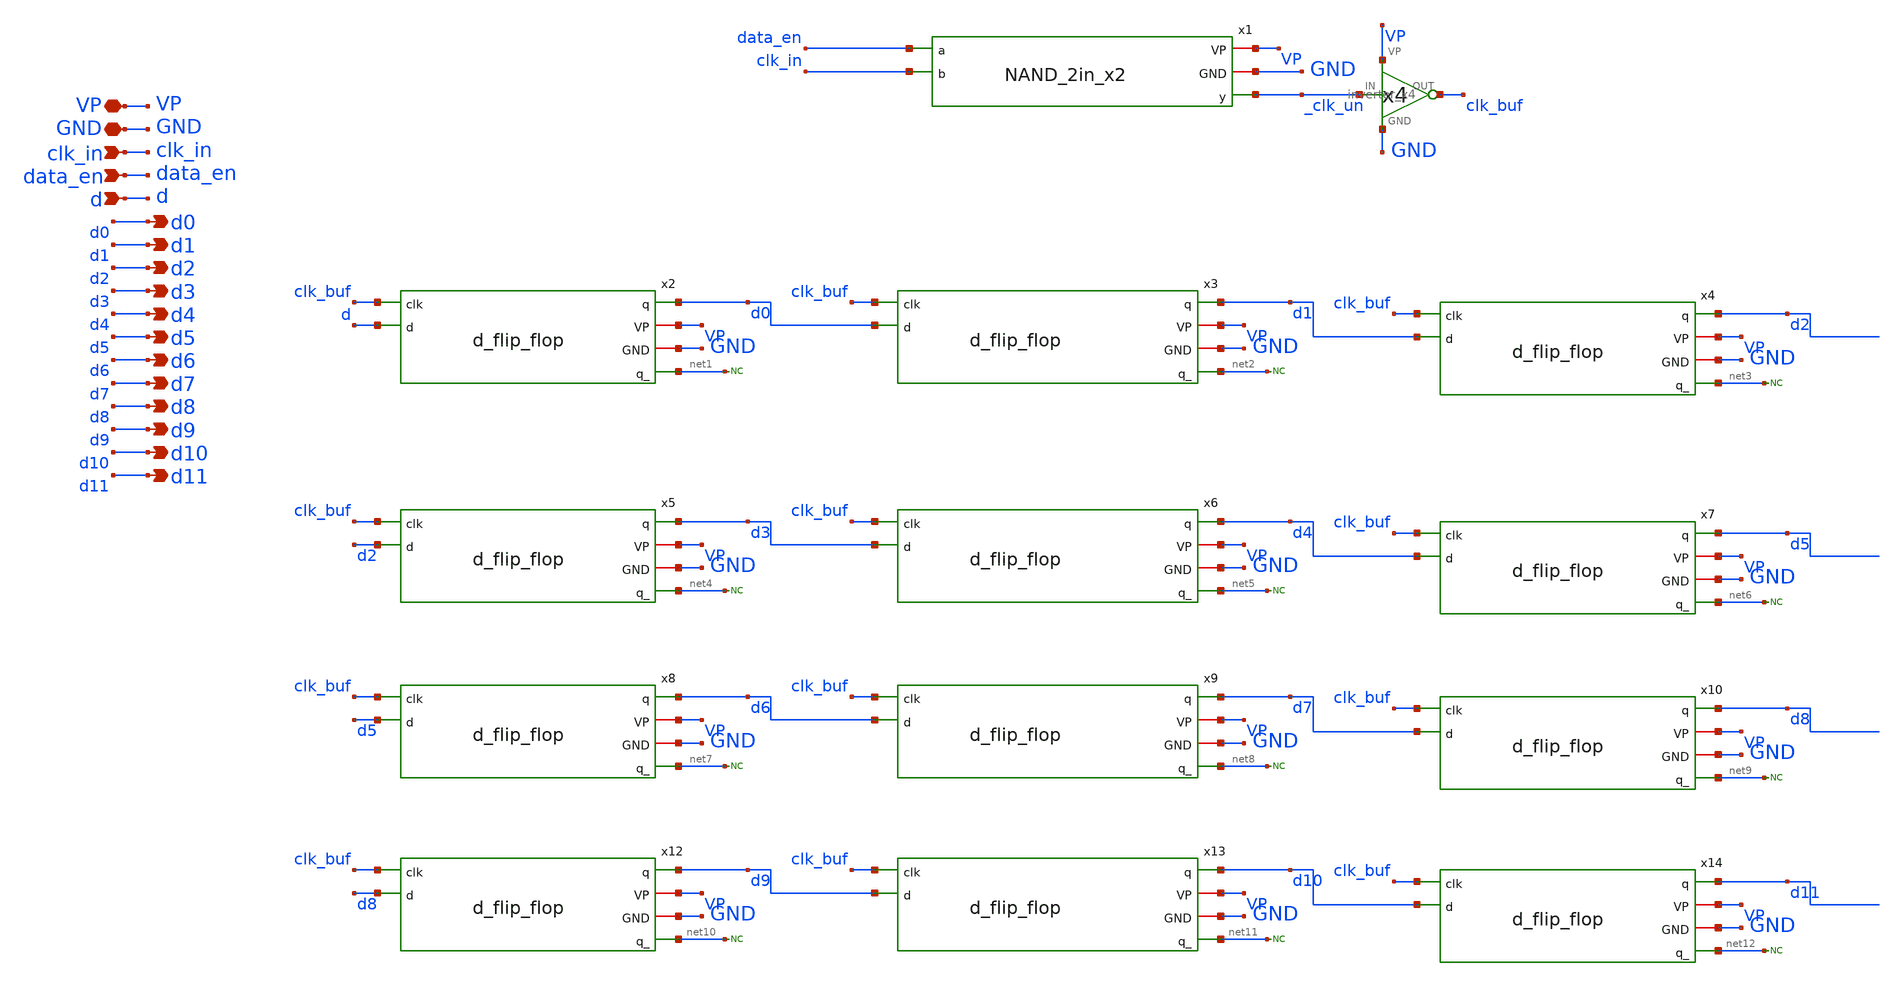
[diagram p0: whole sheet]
** sch_path: PLL0663-main/schematic/xschem/divider/input_register.sch
**.subckt input_register VP clk_in GND data_en d d0 d2 d3 d4 d5 d6 d7 d1 d8 d9 d10 d11
*.iopin VP
*.ipin clk_in
*.iopin GND
*.ipin data_en
*.ipin d
*.opin d0
*.opin d2
*.opin d3
*.opin d4
*.opin d5
*.opin d6
*.opin d7
*.opin d1
*.opin d8
*.opin d9
*.opin d10
*.opin d11
x2 d0 VP GND net1 clk_buf d d_flip_flop
x3 d1 VP GND net2 clk_buf d0 d_flip_flop
x4 d2 VP GND net3 clk_buf d1 d_flip_flop
x5 d3 VP GND net4 clk_buf d2 d_flip_flop
x6 d4 VP GND net5 clk_buf d3 d_flip_flop
x7 d5 VP GND net6 clk_buf d4 d_flip_flop
x8 d6 VP GND net7 clk_buf d5 d_flip_flop
x9 d7 VP GND net8 clk_buf d6 d_flip_flop
x10 d8 VP GND net9 clk_buf d7 d_flip_flop
x11 _clk_un clk_buf VP GND inverter_x4
x12 d9 VP GND net10 clk_buf d8 d_flip_flop
x13 d10 VP GND net11 clk_buf d9 d_flip_flop
x14 d11 VP GND net12 clk_buf d10 d_flip_flop
* noconn #net1
* noconn #net2
* noconn #net3
* noconn #net4
* noconn #net5
* noconn #net6
* noconn #net7
* noconn #net8
* noconn #net9
* noconn #net10
* noconn #net11
* noconn #net12
x1 VP GND data_en _clk_un clk_in NAND_2in_x2
**.ends
.end
